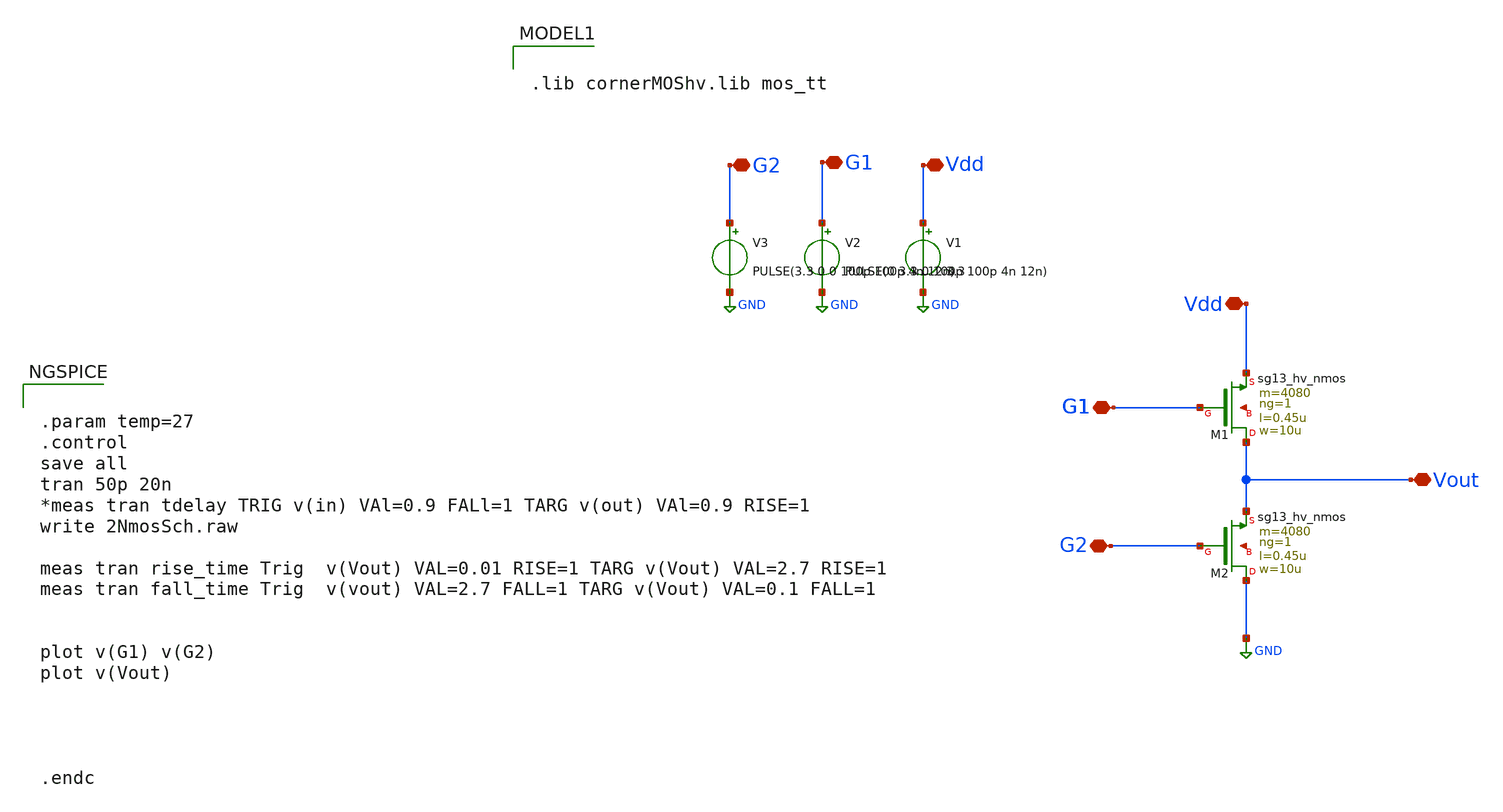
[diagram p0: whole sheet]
** sch_path: Rediseno/SIIIMMM2NmosSch.sch
**.subckt SIIIMMM2NmosSch Vout Vdd G1 G2 G1 G1 G1 G1 G2 Vdd
*.iopin Vout
*.iopin Vdd
*.iopin G1
*.iopin G2
*.iopin G1
*.iopin G1
*.iopin G1
*.iopin G1
*.iopin G2
*.iopin Vdd
XM2 GND G2 Vout net1 sg13_hv_nmos w=10u l=0.45u ng=1 m=4080 mm_ok=1
XM1 Vout G1 Vdd net2 sg13_hv_nmos w=10u l=0.45u ng=1 m=4080 mm_ok=1
V1 Vdd GND 3.3
V2 G1 GND PULSE(0 3.3 0 100p 100p 4n 12n)
V3 G2 GND PULSE(3.3 0 0 100p 100p 4n 12n)
**** begin user architecture code

.lib cornerMOShv.lib mos_tt



.param temp=27
.control
save all
tran 50p 20n
*meas tran tdelay TRIG v(in) VAl=0.9 FALl=1 TARG v(out) VAl=0.9 RISE=1
write 2NmosSch.raw

meas tran rise_time Trig  v(Vout) VAL=0.01 RISE=1 TARG v(Vout) VAL=2.7 RISE=1
meas tran fall_time Trig  v(vout) VAL=2.7 FALL=1 TARG v(Vout) VAL=0.1 FALL=1


plot v(G1) v(G2)
plot v(Vout)




.endc


**** end user architecture code
**.ends
.GLOBAL GND
.end
